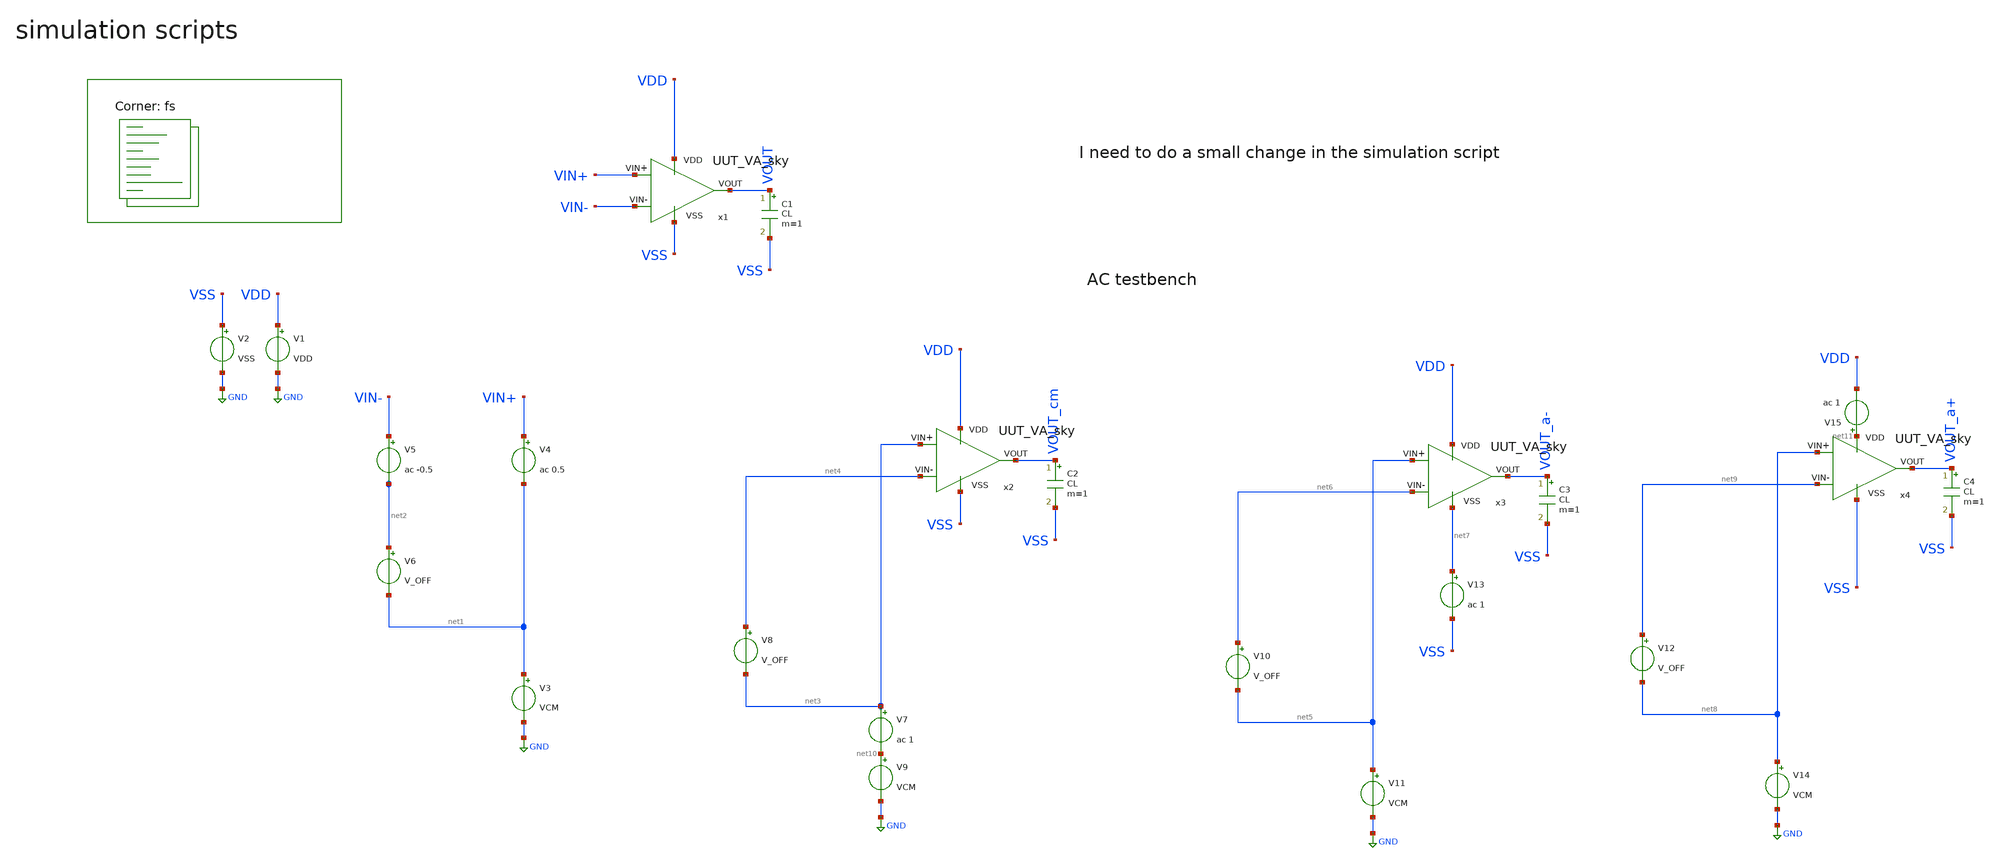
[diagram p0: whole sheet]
** sch_path: Learning/single_ended_amplifiers/Design_and_Analysis_of_Two-Stage_CMOS_Operational_Amplifier_for_Fluorescence_Signal_Processing_sky130_5V/amplifier_design/OTA_AC_TB.sch
**.subckt OTA_AC_TB
V1 VDD GND VDD
V2 VSS GND VSS
V4 VIN+ net1 ac 0.5
V6 net2 net1 V_OFF
V3 net1 GND VCM
C1 VOUT VSS CL m=1
C2 VOUT_cm VSS CL m=1
V8 net4 net3 V_OFF
V9 net10 GND VCM
V7 net3 net10 ac 1
C3 VOUT_a- VSS CL m=1
V10 net6 net5 V_OFF
V11 net5 GND VCM
V13 net7 VSS ac 1
C4 VOUT_a+ VSS CL m=1
V12 net9 net8 V_OFF
V14 net8 GND VCM
V15 net11 VDD ac 1
x1 VDD VSS VIN- VIN+ VOUT UUT_VA_sky
x2 VDD VSS net4 net3 VOUT_cm UUT_VA_sky
x3 VDD net7 net6 net5 VOUT_a- UUT_VA_sky
x4 net11 VSS net9 net8 VOUT_a+ UUT_VA_sky
V5 VIN- net2 ac -0.5
**** begin user architecture code
.lib $::SKYWATER_MODELS/sky130.lib.spice fs

.Temp 27
.param VDD = 1.8
.param VSS = 0
.param VCM={(VDD-VSS)/2}
.param VCM_NEG={-VCM}
.param V_OFF = 900.0m
.param CL = 3p

.control
save all

ac dec 100 1 10G
setseed 10
wrdata VIN_sweep_AC.csv db(v(VOUT)) phase(VOUT) db(v(VOUT_cm)) db(v(VOUT_a-)) db(v(VOUT_a+))
plot db(v(VOUT)) phase(VOUT)
plot db(v(VOUT_cm))
plot db(v(VOUT_a-))
plot db(v(VOUT_a+))

.endc

**** end user architecture code
**.ends

* expanding   symbol:  Sky130A/UUT_sky/UUT_VA_sky.sym # of pins=5
** sym_path: my_ip/LIB/Sky130A/UUT_sky/UUT_VA_sky.sym
** sch_path: my_ip/LIB/Sky130A/UUT_sky/UUT_VA_sky.sch
.subckt UUT_VA_sky VDD VSS VIN- VIN+ VOUT
*.iopin VDD
*.iopin VSS
*.iopin VIN-
*.iopin VIN+
*.iopin VOUT
x1 VDD VSS VIN+ VIN- VOUT A001
.ends

.GLOBAL GND
.end
